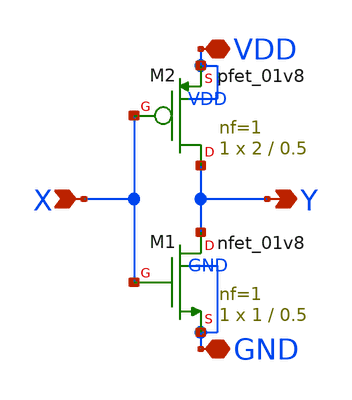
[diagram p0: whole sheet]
** sch_path: Layouts and Schematics/Spice Sim and Schem/inv.sch
**.subckt inv X VDD GND Y
*.ipin X
*.iopin VDD
*.iopin GND
*.opin Y
XM1 Y X GND GND sky130_fd_pr__nfet_01v8 L=0.5 W=1 nf=1 ad='int((nf+1)/2) * W/nf * 0.29' as='int((nf+2)/2) * W/nf * 0.29'
+ pd='2*int((nf+1)/2) * (W/nf + 0.29)' ps='2*int((nf+2)/2) * (W/nf + 0.29)' nrd='0.29 / W' nrs='0.29 / W'
+ sa=0 sb=0 sd=0 mult=1 m=1
XM2 Y X VDD VDD sky130_fd_pr__pfet_01v8 L=0.5 W=2 nf=1 ad='int((nf+1)/2) * W/nf * 0.29' as='int((nf+2)/2) * W/nf * 0.29'
+ pd='2*int((nf+1)/2) * (W/nf + 0.29)' ps='2*int((nf+2)/2) * (W/nf + 0.29)' nrd='0.29 / W' nrs='0.29 / W'
+ sa=0 sb=0 sd=0 mult=1 m=1
**.ends
.end
